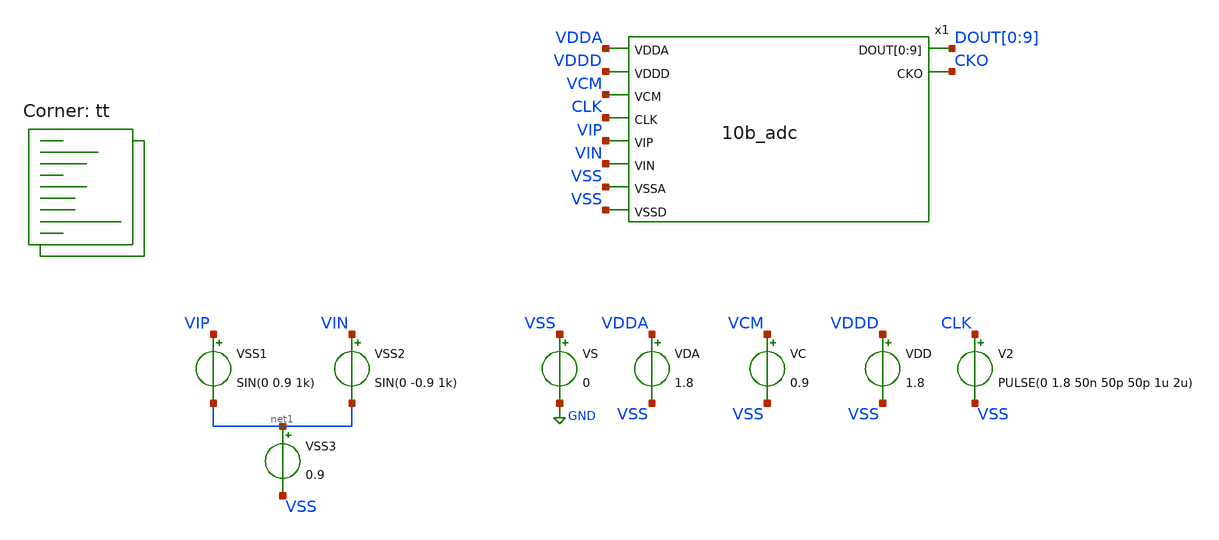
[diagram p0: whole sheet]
** sch_path: xschem/adc_tb.sch
**.subckt adc_tb
VS VSS GND 0
VDA VDDA VSS 1.8
VDD VDDD VSS 1.8
VC VCM VSS 0.9
VSS1 VIP net1 SIN(0 0.9 1k)
VSS2 VIN net1 SIN(0 -0.9 1k)
VSS3 net1 VSS 0.9
V2 CLK VSS PULSE(0 1.8 50n 50p 50p 1u 2u)
x1 VDDA VDDD VCM CLK VIP VIN VSS VSS DOUT[0] DOUT[1] DOUT[2] DOUT[3] DOUT[4] DOUT[5] DOUT[6] DOUT[7]
+ DOUT[8] DOUT[9] CKO 10b_adc
**** begin user architecture code

** opencircuitdesign pdks install
* .lib $::SKYWATER_MODELS/sky130.lib.spice tt
.include /usr/local/share/pdk/sky130A/libs.ref/sky130_fd_sc_hd/spice/sky130_fd_sc_hd.spice



.option wnflag=0
.option savecurrents
.options acct list
.options method=gear
.control
global netlist_dir .
set wr_singlescale
save  clk  vip  vin  x1.vcp  x1.vcn  'dout[0]'  'dout[1]'  'dout[2]'  'dout[3]'  'dout[4]'  'dout[5]'
+  'dout[6]'  'dout[7]'  'dout[8]'  'dout[9]'  cko
tran 100n 2m uic
remzerovec
write adc.raw
.endc

.lib $::SKYWATER_MODELS/sky130.lib.spice tt
**** end user architecture code
**.ends
.GLOBAL GND
.end
